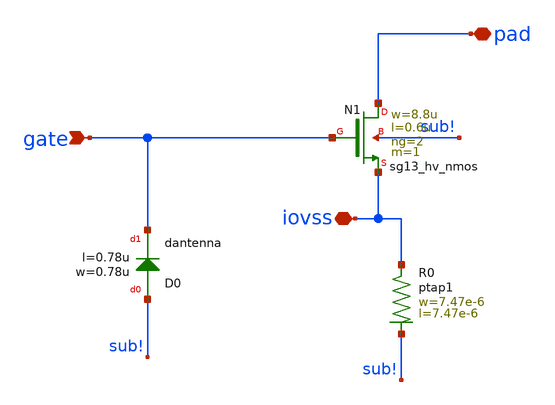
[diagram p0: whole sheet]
** sch_path: ihp-sg13g2/libs.ref/sg13g2_io/sch/xschem/sg13g2_Clamp_N2N2D.sch
**.subckt sg13g2_Clamp_N2N2D pad gate iovss
*.iopin pad
*.ipin gate
*.iopin iovss
XN1 pad gate iovss sub! sg13_hv_nmos w=8.8u l=0.6u ng=2 m=1 mm_ok=1
XD0 sub! gate dantenna l=0.78u w=0.78u
XR0 iovss sub! ptap1 R=11.44 w=7.47e-6 l=7.47e-6
**.ends
.end
